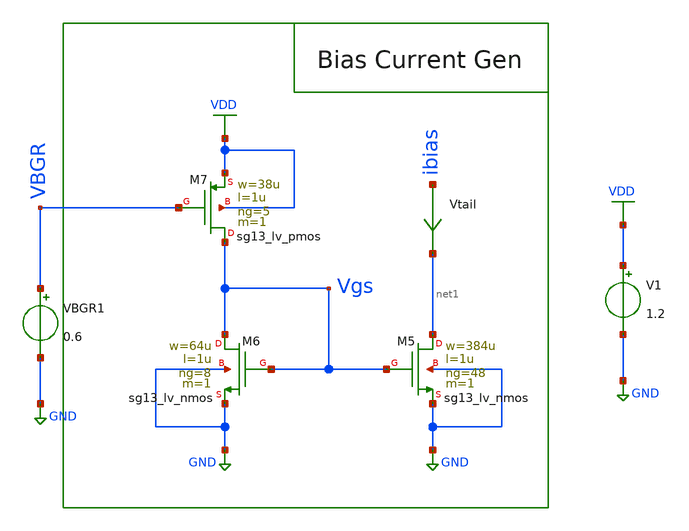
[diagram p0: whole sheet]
** sch_path: schematic/charge-pump/cp_current.sch
**.subckt cp_current
VBGR1 VBGR GND 0.6
XM5 net1 Vgs GND GND sg13_lv_nmos w=384u l=1u ng=48 m=1 mm_ok=1
XM6 Vgs Vgs GND GND sg13_lv_nmos w=64u l=1u ng=8 m=1 mm_ok=1
XM7 Vgs VBGR VDD VDD sg13_lv_pmos w=38u l=1u ng=5 m=1 mm_ok=1
Vtail ibias net1 0
.save i(vtail)
V1 VDD GND 1.2
**** begin user architecture code




.param temp = 27
.options method=gear rshunt=1e12

.control

* Run operating point analysis
op

* Print current through ibias (Vtail source)
print i(Vtail)
tran 1n 1u
plot i(Vtail)

.endc




.lib cornerMOSlv.lib mos_tt
.lib cornerMOShv.lib mos_tt
.lib cornerRES.lib res_typ
.lib cornerCAP.lib cap_typ

**** end user architecture code
**.ends
.GLOBAL GND
.GLOBAL VDD
.end
